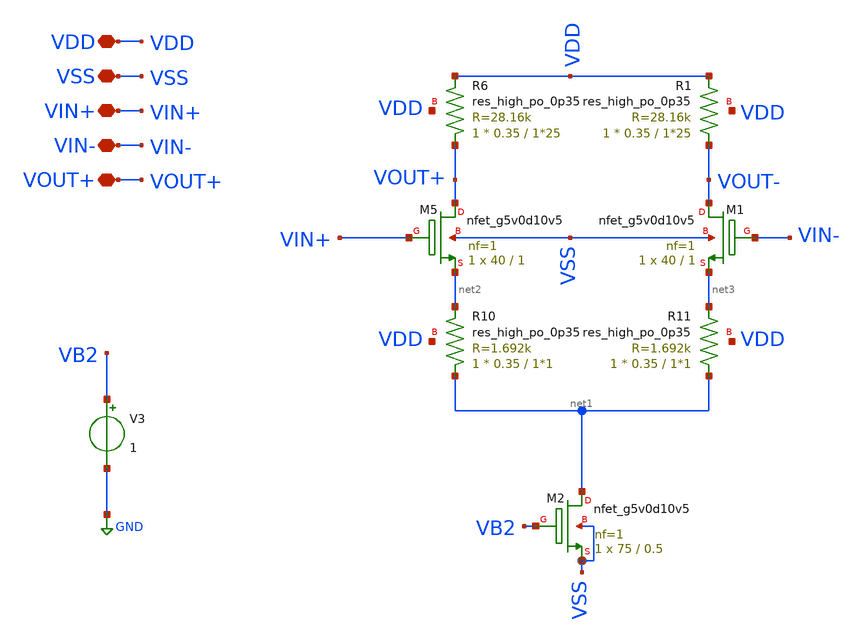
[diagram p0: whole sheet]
** sch_path: amplifiers/differencial_stage_amps/basic_stages/degenerated_stage/differential_stage.sch
**.subckt differential_stage VDD VSS VIN+ VIN- VOUT+
*.iopin VDD
*.iopin VSS
*.iopin VIN+
*.iopin VIN-
*.iopin VOUT+
XM5 VOUT+ VIN+ net2 VSS sky130_fd_pr__nfet_g5v0d10v5 L=1 W=40 nf=1 ad='int((1 + 1)/2) * 40 / 1 * 0.29'
+ as='int((1 + 2)/2) * 40 / 1 * 0.29' pd='2*int((1 + 1)/2) * (40 / 1 + 0.29)' ps='2*int((1 + 2)/2) * (40 / 1 + 0.29)'
+ nrd='0.29 / 40 ' nrs='0.29 / 40 ' sa=0 sb=0 sd=0 mult=1 m=1
XM1 VOUT- VIN- net3 VSS sky130_fd_pr__nfet_g5v0d10v5 L=1 W=40 nf=1 ad='int((1 + 1)/2) * 40 / 1 * 0.29'
+ as='int((1 + 2)/2) * 40 / 1 * 0.29' pd='2*int((1 + 1)/2) * (40 / 1 + 0.29)' ps='2*int((1 + 2)/2) * (40 / 1 + 0.29)'
+ nrd='0.29 / 40 ' nrs='0.29 / 40 ' sa=0 sb=0 sd=0 mult=1 m=1
XR6 VOUT+ VDD VDD sky130_fd_pr__res_high_po_0p35 L=1*25 mult=1 m=1
XR1 VOUT- VDD VDD sky130_fd_pr__res_high_po_0p35 L=1*25 mult=1 m=1
XM2 net1 VB2 VSS VSS sky130_fd_pr__nfet_g5v0d10v5 L=0.5 W=75 nf=1 ad='int((1 + 1)/2) * 75 / 1 * 0.29'
+ as='int((1 + 2)/2) * 75 / 1 * 0.29' pd='2*int((1 + 1)/2) * (75 / 1 + 0.29)' ps='2*int((1 + 2)/2) * (75 / 1 + 0.29)'
+ nrd='0.29 / 75 ' nrs='0.29 / 75 ' sa=0 sb=0 sd=0 mult=1 m=1
V3 VB2 GND 1
XR10 net1 net2 VDD sky130_fd_pr__res_high_po_0p35 L=1*1 mult=1 m=1
XR11 net1 net3 VDD sky130_fd_pr__res_high_po_0p35 L=1*1 mult=1 m=1
**.ends
.GLOBAL GND
.end
